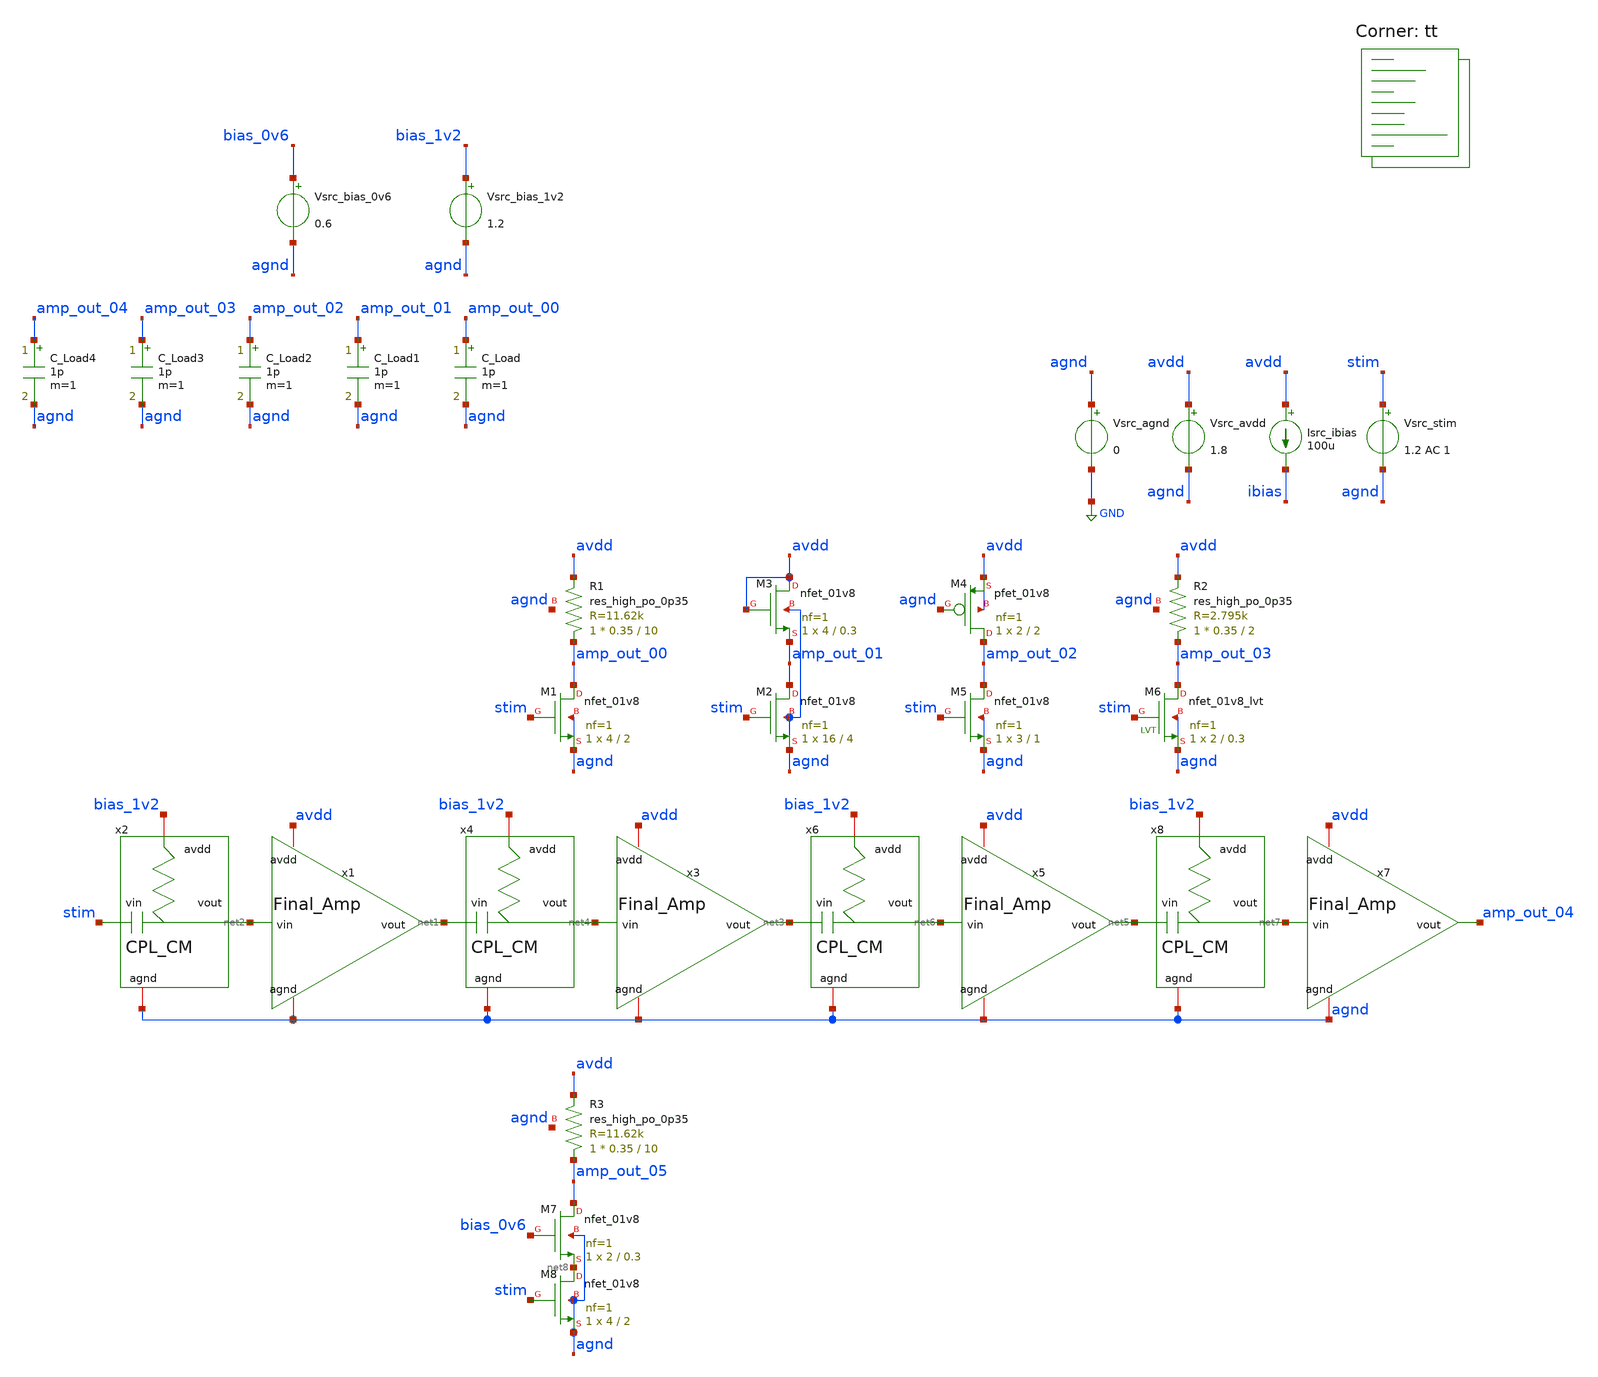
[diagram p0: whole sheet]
** sch_path: AMP/TB_Topologies.sch
**.subckt TB_Topologies
Vsrc_agnd agnd GND 0
Vsrc_avdd avdd agnd 1.8
Vsrc_stim stim agnd 1.2 AC 1
Isrc_ibias avdd ibias 100u
Vsrc_bias_1v2 bias_1v2 agnd 1.2
XM1 amp_out_00 stim agnd agnd sky130_fd_pr__nfet_01v8 L=2 W=4 nf=1 ad='int((nf+1)/2) * W/nf * 0.29' as='int((nf+2)/2) * W/nf * 0.29'
+ pd='2*int((nf+1)/2) * (W/nf + 0.29)' ps='2*int((nf+2)/2) * (W/nf + 0.29)' nrd='0.29 / W' nrs='0.29 / W'
+ sa=0 sb=0 sd=0 mult=1 m=1
XR1 amp_out_00 avdd agnd sky130_fd_pr__res_high_po_0p35 L=10 mult=1 m=1
C_Load amp_out_00 agnd 1p m=1
XM2 amp_out_01 stim agnd agnd sky130_fd_pr__nfet_01v8 L=4 W=16 nf=1 ad='int((nf+1)/2) * W/nf * 0.29'
+ as='int((nf+2)/2) * W/nf * 0.29' pd='2*int((nf+1)/2) * (W/nf + 0.29)' ps='2*int((nf+2)/2) * (W/nf + 0.29)'
+ nrd='0.29 / W' nrs='0.29 / W' sa=0 sb=0 sd=0 mult=1 m=1
XM3 avdd avdd amp_out_01 agnd sky130_fd_pr__nfet_01v8 L=0.3 W=4 nf=1 ad='int((nf+1)/2) * W/nf * 0.29'
+ as='int((nf+2)/2) * W/nf * 0.29' pd='2*int((nf+1)/2) * (W/nf + 0.29)' ps='2*int((nf+2)/2) * (W/nf + 0.29)'
+ nrd='0.29 / W' nrs='0.29 / W' sa=0 sb=0 sd=0 mult=1 m=1
C_Load1 amp_out_01 agnd 1p m=1
XM4 amp_out_02 agnd avdd avdd sky130_fd_pr__pfet_01v8 L=2 W=2 nf=1 ad='int((nf+1)/2) * W/nf * 0.29' as='int((nf+2)/2) * W/nf * 0.29'
+ pd='2*int((nf+1)/2) * (W/nf + 0.29)' ps='2*int((nf+2)/2) * (W/nf + 0.29)' nrd='0.29 / W' nrs='0.29 / W'
+ sa=0 sb=0 sd=0 mult=1 m=1
XM5 amp_out_02 stim agnd agnd sky130_fd_pr__nfet_01v8 L=1 W=3 nf=1 ad='int((nf+1)/2) * W/nf * 0.29' as='int((nf+2)/2) * W/nf * 0.29'
+ pd='2*int((nf+1)/2) * (W/nf + 0.29)' ps='2*int((nf+2)/2) * (W/nf + 0.29)' nrd='0.29 / W' nrs='0.29 / W'
+ sa=0 sb=0 sd=0 mult=1 m=1
XR2 amp_out_03 avdd agnd sky130_fd_pr__res_high_po_0p35 L=2 mult=1 m=1
XM6 amp_out_03 stim agnd agnd sky130_fd_pr__nfet_01v8_lvt L=0.3 W=2 nf=1 ad='int((nf+1)/2) * W/nf * 0.29'
+ as='int((nf+2)/2) * W/nf * 0.29' pd='2*int((nf+1)/2) * (W/nf + 0.29)' ps='2*int((nf+2)/2) * (W/nf + 0.29)'
+ nrd='0.29 / W' nrs='0.29 / W' sa=0 sb=0 sd=0 mult=1 m=1
C_Load2 amp_out_02 agnd 1p m=1
C_Load3 amp_out_03 agnd 1p m=1
x1 net1 net2 agnd avdd Final_Amp
x2 bias_1v2 agnd net2 stim CPL_CM
x3 net3 net4 agnd avdd Final_Amp
x4 bias_1v2 agnd net4 net1 CPL_CM
x5 net5 net6 agnd avdd Final_Amp
x6 bias_1v2 agnd net6 net3 CPL_CM
x7 amp_out_04 net7 agnd avdd Final_Amp
x8 bias_1v2 agnd net7 net5 CPL_CM
C_Load4 amp_out_04 agnd 1p m=1
XM7 amp_out_05 bias_0v6 net8 agnd sky130_fd_pr__nfet_01v8 L=0.3 W=2 nf=1 ad='int((nf+1)/2) * W/nf * 0.29'
+ as='int((nf+2)/2) * W/nf * 0.29' pd='2*int((nf+1)/2) * (W/nf + 0.29)' ps='2*int((nf+2)/2) * (W/nf + 0.29)'
+ nrd='0.29 / W' nrs='0.29 / W' sa=0 sb=0 sd=0 mult=1 m=1
XR3 amp_out_05 avdd agnd sky130_fd_pr__res_high_po_0p35 L=10 mult=1 m=1
XM8 net8 stim agnd agnd sky130_fd_pr__nfet_01v8 L=2 W=4 nf=1 ad='int((nf+1)/2) * W/nf * 0.29' as='int((nf+2)/2) * W/nf * 0.29'
+ pd='2*int((nf+1)/2) * (W/nf + 0.29)' ps='2*int((nf+2)/2) * (W/nf + 0.29)' nrd='0.29 / W' nrs='0.29 / W'
+ sa=0 sb=0 sd=0 mult=1 m=1
Vsrc_bias_0v6 bias_0v6 agnd 0.6
**** begin user architecture code

* this option enables mos model bin
* selection based on W/NF instead of W

.option savecurrents

.control
save all
op

* Print newline
echo

* Print stats for each MOSFET
foreach nmos xm1 xm2 xm3 xm5 x1.xm1 x3.xm1 x5.xm1 x7.xm1 xm7 xm8
 * Save stats
 save @m.{$nmos}.msky130_fd_pr__nfet_01v8[gm]
 let vth   = @m.{$nmos}.msky130_fd_pr__nfet_01v8[vth]
 let vgs   = @m.{$nmos}.msky130_fd_pr__nfet_01v8[vgs]
 let vds   = @m.{$nmos}.msky130_fd_pr__nfet_01v8[vds]
 let vdsat = @m.{$nmos}.msky130_fd_pr__nfet_01v8[vdsat]
 let gm    = @m.{$nmos}.msky130_fd_pr__nfet_01v8[gm]
 let gds   = @m.{$nmos}.msky130_fd_pr__nfet_01v8[gds]


 * Print stats
 echo Stats for $nmos:
 print vth
 print vgs
 print vds
 print vdsat
 print gm
 print gds

 * Print newline
 echo
end

foreach pmos xm4
 * Save stats
 save @m.{$pmos}.msky130_fd_pr__nfet_01v8[gm]
 let vth   = @m.{$pmos}.msky130_fd_pr__pfet_01v8[vth]
 let vgs   = @m.{$pmos}.msky130_fd_pr__pfet_01v8[vgs]
 let vds   = @m.{$pmos}.msky130_fd_pr__pfet_01v8[vds]
 let vdsat = @m.{$pmos}.msky130_fd_pr__pfet_01v8[vdsat]
 let gm    = @m.{$pmos}.msky130_fd_pr__pfet_01v8[gm]
 let gds   = @m.{$pmos}.msky130_fd_pr__pfet_01v8[gds]

 * Print stats
 echo Stats for $pmos:
 print vth
 print vgs
 print vds
 print vdsat
 print gm
 print gds

 * Print newline
 echo
end

foreach nmos xm6
 * Save stats
 save @m.{$nmos}.msky130_fd_pr__nfet_01v8_lvt[gm]
 let vth   = @m.{$nmos}.msky130_fd_pr__nfet_01v8_lvt[vth]
 let vgs   = @m.{$nmos}.msky130_fd_pr__nfet_01v8_lvt[vgs]
 let vds   = @m.{$nmos}.msky130_fd_pr__nfet_01v8_lvt[vds]
 let vdsat = @m.{$nmos}.msky130_fd_pr__nfet_01v8_lvt[vdsat]
 let gm    = @m.{$nmos}.msky130_fd_pr__nfet_01v8_lvt[gm]
 let gds   = @m.{$nmos}.msky130_fd_pr__nfet_01v8_lvt[gds]


 * Print stats
 echo Stats for $nmos:
 print vth
 print vgs
 print vds
 print vdsat
 print gm
 print gds

 * Print newline
 echo
end

* Print region of operation
echo Regions of Operation:
foreach nmos xm1 xm2 xm3 xm5 x1.xm1 x3.xm1 x5.xm1 x7.xm1 xm7 xm8
 * Save stats
 let vds = @m.{$nmos}.msky130_fd_pr__nfet_01v8[vds]
 let vgs = @m.{$nmos}.msky130_fd_pr__nfet_01v8[vgs]
 let vth = @m.{$nmos}.msky130_fd_pr__nfet_01v8[vth]

 * Check and print regions
 if (vgs <= vth)
  echo $nmos: N Cutoff
  print vgs
  print vth
 end
 if (vgs > vth) & (vds <= (vgs - vth))
  echo $nmos: N Triode
  print vgs
  print vth
  print vds
 end
 if (vgs > vth) & (vds > (vgs - vth))
  echo $nmos: N Saturation
 end
end

foreach pmos xm4
 * Save stats
 let vds = @m.{$pmos}.msky130_fd_pr__pfet_01v8[vds]
 let vgs = @m.{$pmos}.msky130_fd_pr__pfet_01v8[vgs]
 let vth = @m.{$pmos}.msky130_fd_pr__pfet_01v8[vth]

 * Check and print regions
 if (abs(vgs) <= abs(vth))
  echo $pmos: P Cutoff
  print vgs
  print vth
 end
 if (abs(vgs) > abs(vth)) & (abs(vds) <= (abs(vgs) - abs(vth)))
  echo $pmos: P Triode
  print vgs
  print vth
  print vds
 end
 if (abs(vgs) > abs(vth)) & (abs(vds) > (abs(vgs) - abs(vth)))
  echo $pmos: P Saturation
 end
end

* Print region of operation
foreach nmos xm6
 * Save stats
 let vds = @m.{$nmos}.msky130_fd_pr__nfet_01v8_lvt[vds]
 let vgs = @m.{$nmos}.msky130_fd_pr__nfet_01v8_lvt[vgs]
 let vth = @m.{$nmos}.msky130_fd_pr__nfet_01v8_lvt[vth]

 * Check and print regions
 if (vgs <= vth)
  echo $nmos: N Cutoff
  print vgs
  print vth
 end
 if (vgs > vth) & (vds <= (vgs - vth))
  echo $nmos: N Triode
  print vgs
  print vth
  print vds
 end
 if (vgs > vth) & (vds > (vgs - vth))
  echo $nmos: N Saturation
 end
end

* Print newline
echo

* Sweep frequency
write TB_Topologies.raw
set appendwrite
ac dec 100 1 1e11
remzerovec

* Calculate gain
let ratio_00 = v(amp_out_00)/v(stim)
let ratio_01 = v(amp_out_01)/v(stim)
let ratio_02 = v(amp_out_02)/v(stim)
let ratio_03 = v(amp_out_03)/v(stim)
let ratio_04 = v(amp_out_04)/v(stim)
let ratio_05 = v(amp_out_05)/v(stim)

let gain_00 = db(mag(ratio_00))
let gain_01 = db(mag(ratio_01))
let gain_02 = db(mag(ratio_02))
let gain_03 = db(mag(ratio_03))
let gain_04 = db(mag(ratio_04))
let gain_05 = db(mag(ratio_05))

write TB_Topologies.raw

.endc


.lib $::SKYWATER_MODELS/sky130.lib.spice tt
**** end user architecture code
**.ends
.GLOBAL GND
.end
